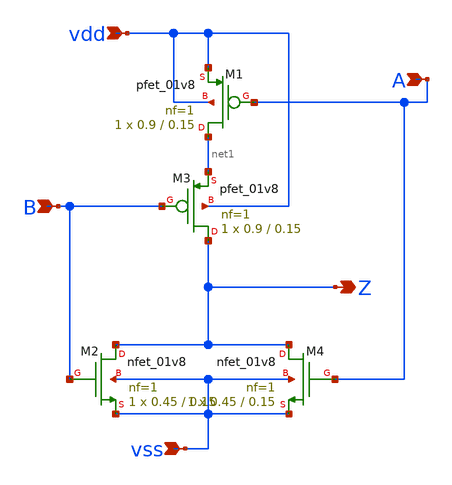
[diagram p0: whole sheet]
** sch_path: track_vlsi/lado/sch/nor.sch
**.subckt nor Z vdd B vss A
*.opin Z
*.ipin vdd
*.ipin B
*.ipin vss
*.ipin A
XM1 net1 A vdd vdd sky130_fd_pr__pfet_01v8 L=0.15 W=0.9 nf=1 ad='int((nf+1)/2) * W/nf * 0.29' as='int((nf+2)/2) * W/nf * 0.29'
+ pd='2*int((nf+1)/2) * (W/nf + 0.29)' ps='2*int((nf+2)/2) * (W/nf + 0.29)' nrd='0.29 / W' nrs='0.29 / W'
+ sa=0 sb=0 sd=0 mult=1 m=1
XM2 Z B vss vss sky130_fd_pr__nfet_01v8 L=0.15 W=0.45 nf=1 ad='int((nf+1)/2) * W/nf * 0.29' as='int((nf+2)/2) * W/nf * 0.29'
+ pd='2*int((nf+1)/2) * (W/nf + 0.29)' ps='2*int((nf+2)/2) * (W/nf + 0.29)' nrd='0.29 / W' nrs='0.29 / W'
+ sa=0 sb=0 sd=0 mult=1 m=1
XM3 Z B net1 vdd sky130_fd_pr__pfet_01v8 L=0.15 W=0.9 nf=1 ad='int((nf+1)/2) * W/nf * 0.29' as='int((nf+2)/2) * W/nf * 0.29'
+ pd='2*int((nf+1)/2) * (W/nf + 0.29)' ps='2*int((nf+2)/2) * (W/nf + 0.29)' nrd='0.29 / W' nrs='0.29 / W'
+ sa=0 sb=0 sd=0 mult=1 m=1
XM4 Z A vss vss sky130_fd_pr__nfet_01v8 L=0.15 W=0.45 nf=1 ad='int((nf+1)/2) * W/nf * 0.29' as='int((nf+2)/2) * W/nf * 0.29'
+ pd='2*int((nf+1)/2) * (W/nf + 0.29)' ps='2*int((nf+2)/2) * (W/nf + 0.29)' nrd='0.29 / W' nrs='0.29 / W'
+ sa=0 sb=0 sd=0 mult=1 m=1
**.ends
.end
